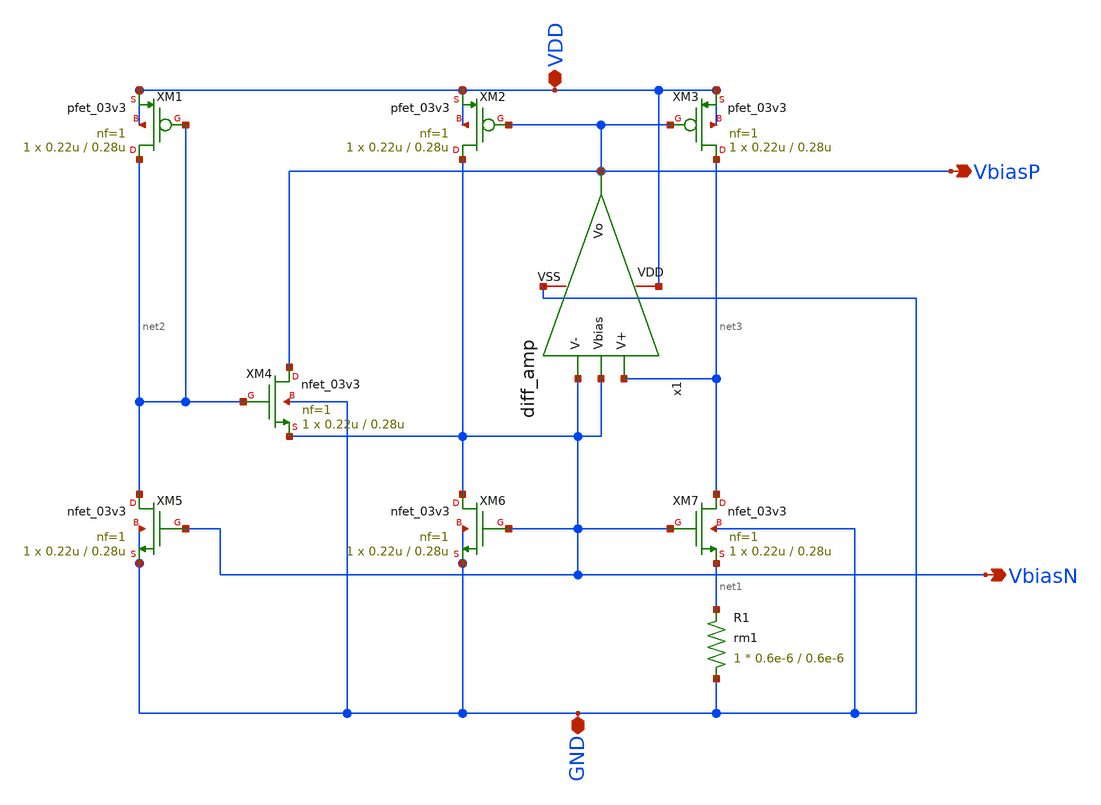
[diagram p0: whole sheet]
** sch_path: analog/beta_multiplier_reference.sch
**.subckt beta_multiplier_reference VDD GND VbiasP VbiasN
*.iopin VDD
*.iopin GND
*.opin VbiasP
*.opin VbiasN
XM1 net2 net2 VDD VDD pfet_03v3 L=0.28u W=0.22u nf=1 ad='int((nf+1)/2) * W/nf * 0.18u' as='int((nf+2)/2) * W/nf * 0.18u'
+ pd='2*int((nf+1)/2) * (W/nf + 0.18u)' ps='2*int((nf+2)/2) * (W/nf + 0.18u)' nrd='0.18u / W' nrs='0.18u / W'
+ sa=0 sb=0 sd=0 m=1
XM2 VbiasN VbiasP VDD VDD pfet_03v3 L=0.28u W=0.22u nf=1 ad='int((nf+1)/2) * W/nf * 0.18u' as='int((nf+2)/2) * W/nf * 0.18u'
+ pd='2*int((nf+1)/2) * (W/nf + 0.18u)' ps='2*int((nf+2)/2) * (W/nf + 0.18u)' nrd='0.18u / W' nrs='0.18u / W'
+ sa=0 sb=0 sd=0 m=1
XM3 net3 VbiasP VDD VDD pfet_03v3 L=0.28u W=0.22u nf=1 ad='int((nf+1)/2) * W/nf * 0.18u' as='int((nf+2)/2) * W/nf * 0.18u'
+ pd='2*int((nf+1)/2) * (W/nf + 0.18u)' ps='2*int((nf+2)/2) * (W/nf + 0.18u)' nrd='0.18u / W' nrs='0.18u / W'
+ sa=0 sb=0 sd=0 m=1
XM4 VbiasP net2 VbiasN GND nfet_03v3 L=0.28u W=0.22u nf=1 ad='int((nf+1)/2) * W/nf * 0.18u' as='int((nf+2)/2) * W/nf * 0.18u'
+ pd='2*int((nf+1)/2) * (W/nf + 0.18u)' ps='2*int((nf+2)/2) * (W/nf + 0.18u)' nrd='0.18u / W' nrs='0.18u / W'
+ sa=0 sb=0 sd=0 m=1
XM5 net2 VbiasN GND GND nfet_03v3 L=0.28u W=0.22u nf=1 ad='int((nf+1)/2) * W/nf * 0.18u' as='int((nf+2)/2) * W/nf * 0.18u'
+ pd='2*int((nf+1)/2) * (W/nf + 0.18u)' ps='2*int((nf+2)/2) * (W/nf + 0.18u)' nrd='0.18u / W' nrs='0.18u / W'
+ sa=0 sb=0 sd=0 m=1
XM6 VbiasN VbiasN GND GND nfet_03v3 L=0.28u W=0.22u nf=1 ad='int((nf+1)/2) * W/nf * 0.18u' as='int((nf+2)/2) * W/nf * 0.18u'
+ pd='2*int((nf+1)/2) * (W/nf + 0.18u)' ps='2*int((nf+2)/2) * (W/nf + 0.18u)' nrd='0.18u / W' nrs='0.18u / W'
+ sa=0 sb=0 sd=0 m=1
XM7 net3 VbiasN net1 GND nfet_03v3 L=0.28u W=0.22u nf=1 ad='int((nf+1)/2) * W/nf * 0.18u' as='int((nf+2)/2) * W/nf * 0.18u'
+ pd='2*int((nf+1)/2) * (W/nf + 0.18u)' ps='2*int((nf+2)/2) * (W/nf + 0.18u)' nrd='0.18u / W' nrs='0.18u / W'
+ sa=0 sb=0 sd=0 m=1
XR1 GND net1 rm1 r_width=0.6e-6 r_length=0.6e-6 m=1
x1 VDD VbiasP net3 VbiasN VbiasN GND diff_amp
**.ends

* expanding   symbol:  AURA/diff_amp.sym # of pins=6
** sym_path: analog/diff_amp.sym
** sch_path: analog/diff_amp.sch
.subckt diff_amp VDD Vo V+ V- Vbias VSS
*.iopin VDD
*.iopin VSS
*.ipin V+
*.ipin V-
*.opin Vo
*.ipin Vbias
XM1 net1 V+ net2 VSS nfet_03v3 L=0.28u W=0.22u nf=1 ad='int((nf+1)/2) * W/nf * 0.18u' as='int((nf+2)/2) * W/nf * 0.18u'
+ pd='2*int((nf+1)/2) * (W/nf + 0.18u)' ps='2*int((nf+2)/2) * (W/nf + 0.18u)' nrd='0.18u / W' nrs='0.18u / W'
+ sa=0 sb=0 sd=0 m=1
XM2 net2 Vbias VSS VSS nfet_03v3 L=0.28u W=0.22u nf=1 ad='int((nf+1)/2) * W/nf * 0.18u' as='int((nf+2)/2) * W/nf * 0.18u'
+ pd='2*int((nf+1)/2) * (W/nf + 0.18u)' ps='2*int((nf+2)/2) * (W/nf + 0.18u)' nrd='0.18u / W' nrs='0.18u / W'
+ sa=0 sb=0 sd=0 m=1
XM3 Vo V- net2 VSS nfet_03v3 L=0.28u W=0.22u nf=1 ad='int((nf+1)/2) * W/nf * 0.18u' as='int((nf+2)/2) * W/nf * 0.18u'
+ pd='2*int((nf+1)/2) * (W/nf + 0.18u)' ps='2*int((nf+2)/2) * (W/nf + 0.18u)' nrd='0.18u / W' nrs='0.18u / W'
+ sa=0 sb=0 sd=0 m=1
XM4 Vo net1 VDD VDD pfet_03v3 L=0.28u W=0.22u nf=1 ad='int((nf+1)/2) * W/nf * 0.18u' as='int((nf+2)/2) * W/nf * 0.18u'
+ pd='2*int((nf+1)/2) * (W/nf + 0.18u)' ps='2*int((nf+2)/2) * (W/nf + 0.18u)' nrd='0.18u / W' nrs='0.18u / W'
+ sa=0 sb=0 sd=0 m=1
XM5 net1 net1 VDD VDD pfet_03v3 L=0.28u W=0.22u nf=1 ad='int((nf+1)/2) * W/nf * 0.18u' as='int((nf+2)/2) * W/nf * 0.18u'
+ pd='2*int((nf+1)/2) * (W/nf + 0.18u)' ps='2*int((nf+2)/2) * (W/nf + 0.18u)' nrd='0.18u / W' nrs='0.18u / W'
+ sa=0 sb=0 sd=0 m=1
.ends

.end
